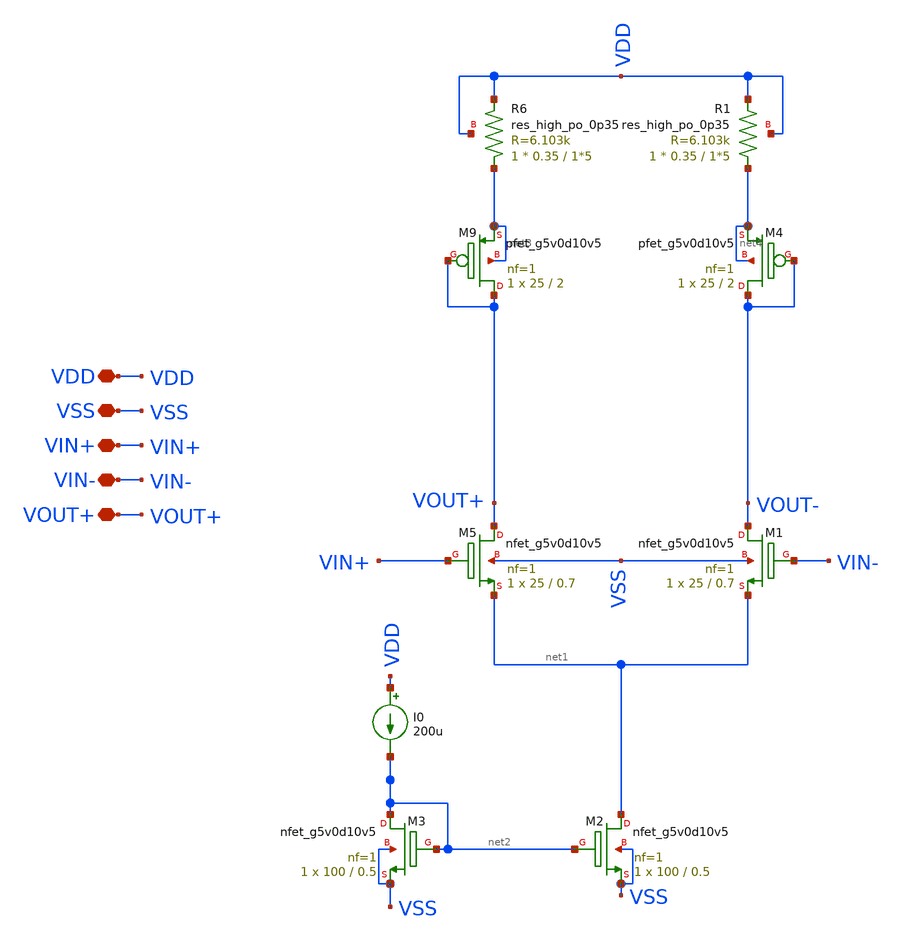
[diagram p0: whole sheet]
** sch_path: old stuff/amplifiers/differencial_stage_amps/stange stages/extra_resistive/differential_stage.sch
**.subckt differential_stage VDD VSS VIN+ VIN- VOUT+
*.iopin VDD
*.iopin VSS
*.iopin VIN+
*.iopin VIN-
*.iopin VOUT+
XM5 VOUT+ VIN+ net1 VSS sky130_fd_pr__nfet_g5v0d10v5 L=0.7 W=25 nf=1 ad='int((1 + 1)/2) * 25 / 1 * 0.29'
+ as='int((1 + 2)/2) * 25 / 1 * 0.29' pd='2*int((1 + 1)/2) * (25 / 1 + 0.29)' ps='2*int((1 + 2)/2) * (25 / 1 + 0.29)'
+ nrd='0.29 / 25 ' nrs='0.29 / 25 ' sa=0 sb=0 sd=0 mult=1 m=1
XM1 VOUT- VIN- net1 VSS sky130_fd_pr__nfet_g5v0d10v5 L=0.7 W=25 nf=1 ad='int((1 + 1)/2) * 25 / 1 * 0.29'
+ as='int((1 + 2)/2) * 25 / 1 * 0.29' pd='2*int((1 + 1)/2) * (25 / 1 + 0.29)' ps='2*int((1 + 2)/2) * (25 / 1 + 0.29)'
+ nrd='0.29 / 25 ' nrs='0.29 / 25 ' sa=0 sb=0 sd=0 mult=1 m=1
XM2 net1 net2 VSS VSS sky130_fd_pr__nfet_g5v0d10v5 L=0.5 W=100 nf=1 ad='int((1 + 1)/2) * 100 / 1 * 0.29'
+ as='int((1 + 2)/2) * 100 / 1 * 0.29' pd='2*int((1 + 1)/2) * (100 / 1 + 0.29)' ps='2*int((1 + 2)/2) * (100 / 1 + 0.29)'
+ nrd='0.29 / 100 ' nrs='0.29 / 100 ' sa=0 sb=0 sd=0 mult=1 m=1
XM3 net2 net2 VSS VSS sky130_fd_pr__nfet_g5v0d10v5 L=0.5 W=100 nf=1 ad='int((1 + 1)/2) * 100 / 1 * 0.29'
+ as='int((1 + 2)/2) * 100 / 1 * 0.29' pd='2*int((1 + 1)/2) * (100 / 1 + 0.29)' ps='2*int((1 + 2)/2) * (100 / 1 + 0.29)'
+ nrd='0.29 / 100 ' nrs='0.29 / 100 ' sa=0 sb=0 sd=0 mult=1 m=1
I0 VDD net2 200u
XM9 VOUT+ VOUT+ net3 net3 sky130_fd_pr__pfet_g5v0d10v5 L=2 W=25 nf=1 ad='int((1 + 1)/2) * 25 / 1 * 0.29'
+ as='int((1 + 2)/2) * 25 / 1 * 0.29' pd='2*int((1 + 1)/2) * (25 / 1 + 0.29)' ps='2*int((1 + 2)/2) * (25 / 1 + 0.29)'
+ nrd='0.29 / 25 ' nrs='0.29 / 25 ' sa=0 sb=0 sd=0 mult=1 m=1
XM4 VOUT- VOUT- net4 net4 sky130_fd_pr__pfet_g5v0d10v5 L=2 W=25 nf=1 ad='int((1 + 1)/2) * 25 / 1 * 0.29'
+ as='int((1 + 2)/2) * 25 / 1 * 0.29' pd='2*int((1 + 1)/2) * (25 / 1 + 0.29)' ps='2*int((1 + 2)/2) * (25 / 1 + 0.29)'
+ nrd='0.29 / 25 ' nrs='0.29 / 25 ' sa=0 sb=0 sd=0 mult=1 m=1
XR6 net3 VDD VDD sky130_fd_pr__res_high_po_0p35 L=1*5 mult=1 m=1
XR1 net4 VDD VDD sky130_fd_pr__res_high_po_0p35 L=1*5 mult=1 m=1
**.ends
.end
